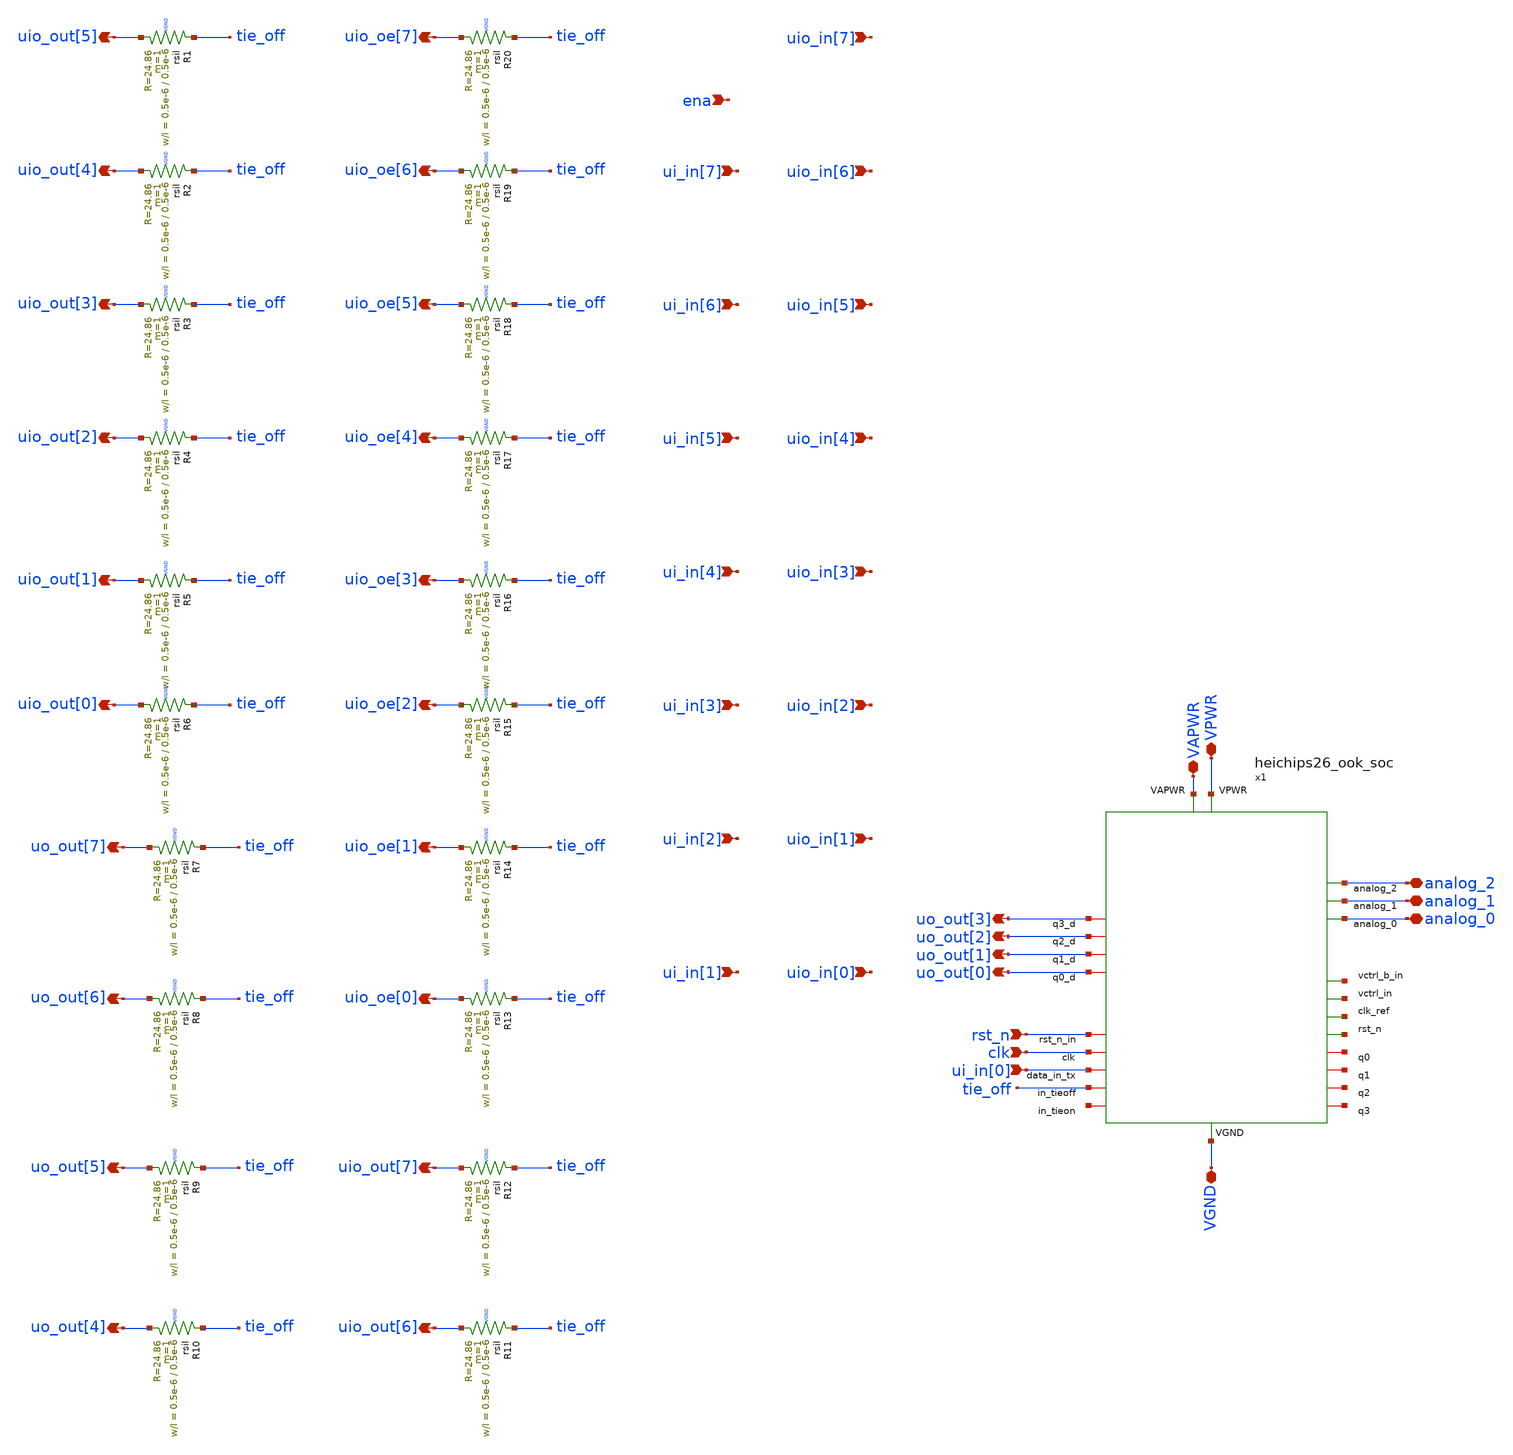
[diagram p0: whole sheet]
** sch_path: macros/heichips26_ook_top/schematic/xschem/heichips26_ook_top.sch
**.subckt heichips26_ook_top VPWR VGND VAPWR analog_2 analog_1 analog_0 uo_out[1] uo_out[2]
*+ uo_out[3] rst_n clk ui_in[0] uo_out[4] uo_out[5] uo_out[6] uo_out[7] uio_out[0] uio_out[1] uio_out[2]
*+ uio_out[3] uio_out[4] uio_out[5] uio_out[6] uio_out[7] uio_oe[0] uio_oe[1] uio_oe[2] uio_oe[3] uio_oe[4]
*+ uio_oe[5] uio_oe[6] uio_oe[7] ui_in[1] ui_in[2] ui_in[3] ui_in[4] ui_in[5] ui_in[6] ui_in[7] uo_out[0] ena
*+ uio_in[0] uio_in[1] uio_in[2] uio_in[3] uio_in[4] uio_in[5] uio_in[6] uio_in[7]
*.iopin VPWR
*.iopin VGND
*.iopin VAPWR
*.iopin analog_2
*.iopin analog_1
*.iopin analog_0
*.opin uo_out[1]
*.opin uo_out[2]
*.opin uo_out[3]
*.ipin rst_n
*.ipin clk
*.ipin ui_in[0]
*.opin uo_out[4]
*.opin uo_out[5]
*.opin uo_out[6]
*.opin uo_out[7]
*.opin uio_out[0]
*.opin uio_out[1]
*.opin uio_out[2]
*.opin uio_out[3]
*.opin uio_out[4]
*.opin uio_out[5]
*.opin uio_out[6]
*.opin uio_out[7]
*.opin uio_oe[0]
*.opin uio_oe[1]
*.opin uio_oe[2]
*.opin uio_oe[3]
*.opin uio_oe[4]
*.opin uio_oe[5]
*.opin uio_oe[6]
*.opin uio_oe[7]
*.ipin ui_in[1]
*.ipin ui_in[2]
*.ipin ui_in[3]
*.ipin ui_in[4]
*.ipin ui_in[5]
*.ipin ui_in[6]
*.ipin ui_in[7]
*.opin uo_out[0]
*.ipin ena
*.ipin uio_in[0]
*.ipin uio_in[1]
*.ipin uio_in[2]
*.ipin uio_in[3]
*.ipin uio_in[4]
*.ipin uio_in[5]
*.ipin uio_in[6]
*.ipin uio_in[7]
x1 VAPWR VPWR VGND analog_2 analog_1 analog_0 net1 net2 net3 net4 net5 net6 net7 net8 uo_out[3]
+ uo_out[2] uo_out[1] uo_out[0] rst_n clk ui_in[0] tie_off net9 heichips26_ook_soc
XR1 tie_off uio_out[5] VGND rsil w=0.5e-6 l=0.5e-6 m=1 mm_ok=1
XR2 tie_off uio_out[4] VGND rsil w=0.5e-6 l=0.5e-6 m=1 mm_ok=1
XR3 tie_off uio_out[3] VGND rsil w=0.5e-6 l=0.5e-6 m=1 mm_ok=1
XR4 tie_off uio_out[2] VGND rsil w=0.5e-6 l=0.5e-6 m=1 mm_ok=1
XR5 tie_off uio_out[1] VGND rsil w=0.5e-6 l=0.5e-6 m=1 mm_ok=1
XR6 tie_off uio_out[0] VGND rsil w=0.5e-6 l=0.5e-6 m=1 mm_ok=1
XR7 tie_off uo_out[7] VGND rsil w=0.5e-6 l=0.5e-6 m=1 mm_ok=1
XR8 tie_off uo_out[6] VGND rsil w=0.5e-6 l=0.5e-6 m=1 mm_ok=1
XR9 tie_off uo_out[5] VGND rsil w=0.5e-6 l=0.5e-6 m=1 mm_ok=1
XR10 tie_off uo_out[4] VGND rsil w=0.5e-6 l=0.5e-6 m=1 mm_ok=1
XR11 tie_off uio_out[6] VGND rsil w=0.5e-6 l=0.5e-6 m=1 mm_ok=1
XR12 tie_off uio_out[7] VGND rsil w=0.5e-6 l=0.5e-6 m=1 mm_ok=1
XR13 tie_off uio_oe[0] VGND rsil w=0.5e-6 l=0.5e-6 m=1 mm_ok=1
XR14 tie_off uio_oe[1] VGND rsil w=0.5e-6 l=0.5e-6 m=1 mm_ok=1
XR15 tie_off uio_oe[2] VGND rsil w=0.5e-6 l=0.5e-6 m=1 mm_ok=1
XR16 tie_off uio_oe[3] VGND rsil w=0.5e-6 l=0.5e-6 m=1 mm_ok=1
XR17 tie_off uio_oe[4] VGND rsil w=0.5e-6 l=0.5e-6 m=1 mm_ok=1
XR18 tie_off uio_oe[5] VGND rsil w=0.5e-6 l=0.5e-6 m=1 mm_ok=1
XR19 tie_off uio_oe[6] VGND rsil w=0.5e-6 l=0.5e-6 m=1 mm_ok=1
XR20 tie_off uio_oe[7] VGND rsil w=0.5e-6 l=0.5e-6 m=1 mm_ok=1
**.ends
.end
